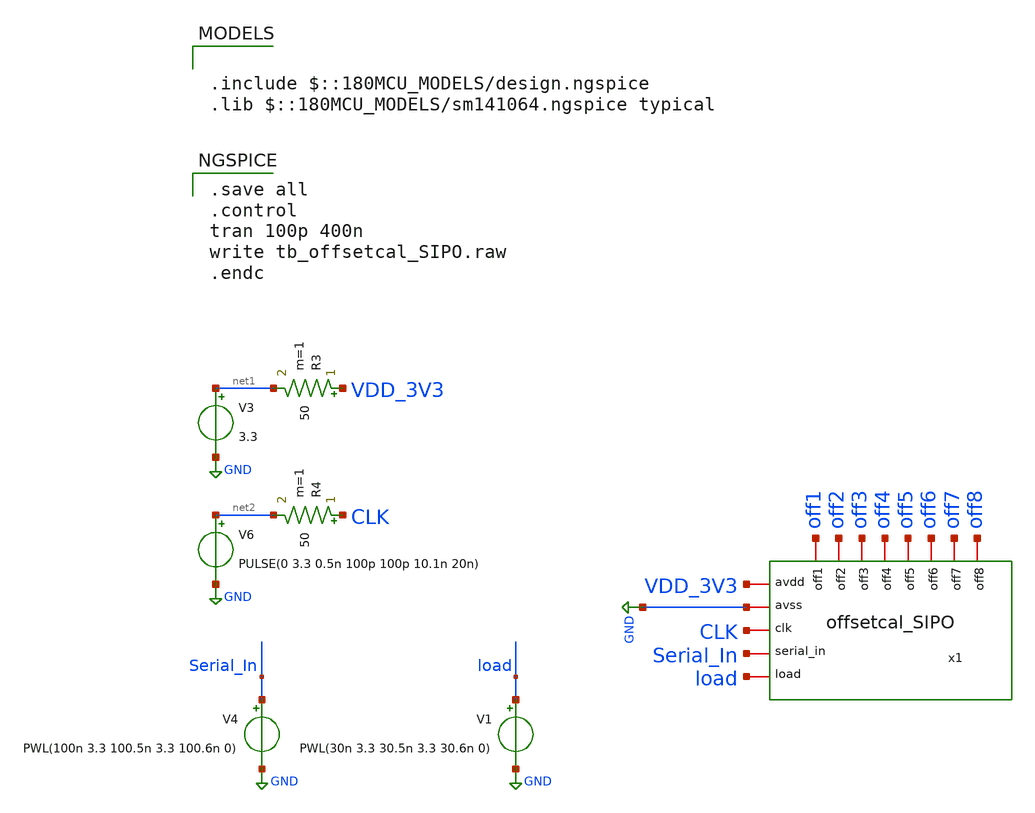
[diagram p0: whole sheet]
** sch_path: designs/libs/SIPO/tb_offsetcal_SIPO.sch
**.subckt tb_offsetcal_SIPO
x1 VDD_3V3 GND off4 off2 off6 off5 off1 off7 off8 off3 Serial_In CLK load offsetcal_SIPO
V3 net1 GND 3.3
V6 net2 GND PULSE(0 3.3 0.5n 100p 100p 10.1n 20n)
R3 VDD_3V3 net1 50 m=1
R4 CLK net2 50 m=1
V4 Serial_In GND PWL(100n 3.3 100.5n 3.3 100.6n 0)
V1 load GND PWL(30n 3.3 30.5n 3.3 30.6n 0)
**** begin user architecture code

.include $::180MCU_MODELS/design.ngspice
.lib $::180MCU_MODELS/sm141064.ngspice typical


.save all
.control
tran 100p 400n
write tb_offsetcal_SIPO.raw
.endc

**** end user architecture code
**.ends
.GLOBAL GND
.end
